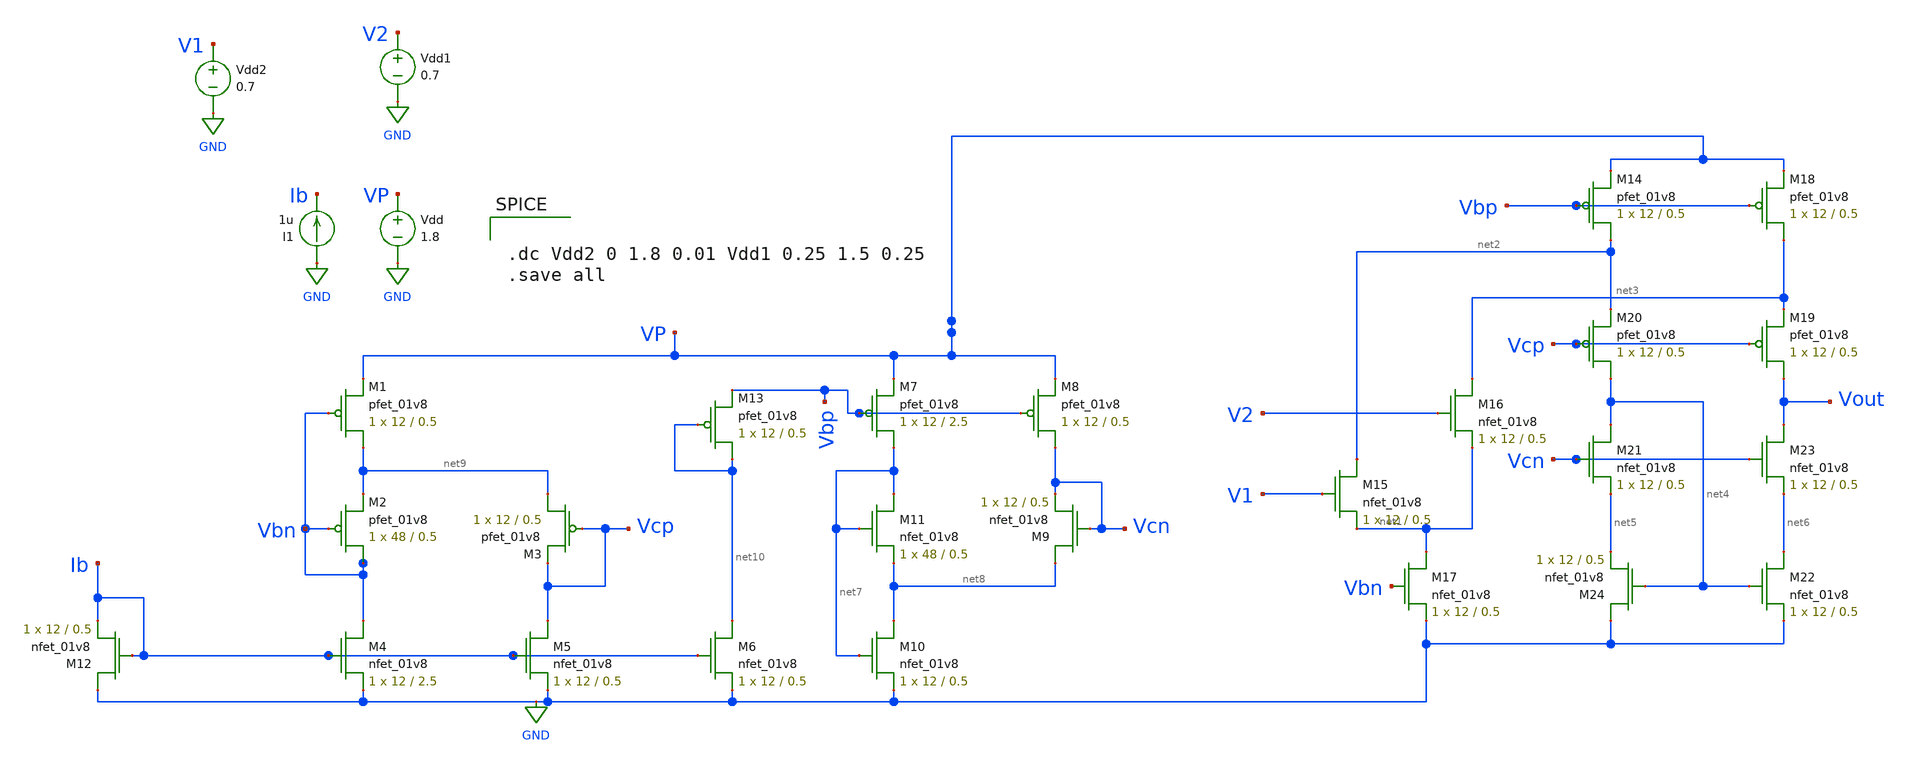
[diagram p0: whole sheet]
** sch_path: mp3/schematic/bias_circuit.sch
**.subckt bias_circuit
I1 GND Ib 1u
Vdd VP GND 1.8
XM14 net2 Vbp VP VDD sky130_fd_pr__pfet_01v8 L=0.5 W=12 nf=1 ad='int((nf+1)/2) * W/nf * 0.29' as='int((nf+2)/2) * W/nf * 0.29'
+ pd='2*int((nf+1)/2) * (W/nf + 0.29)' ps='2*int((nf+2)/2) * (W/nf + 0.29)' nrd='0.29 / W' nrs='0.29 / W'
+ sa=0 sb=0 sd=0 mult=1 m=1
XM15 net2 V1 net1 GND sky130_fd_pr__nfet_01v8 L=0.5 W=12 nf=1 ad='int((nf+1)/2) * W/nf * 0.29' as='int((nf+2)/2) * W/nf * 0.29'
+ pd='2*int((nf+1)/2) * (W/nf + 0.29)' ps='2*int((nf+2)/2) * (W/nf + 0.29)' nrd='0.29 / W' nrs='0.29 / W'
+ sa=0 sb=0 sd=0 mult=1 m=1
XM16 net3 V2 net1 GND sky130_fd_pr__nfet_01v8 L=0.5 W=12 nf=1 ad='int((nf+1)/2) * W/nf * 0.29' as='int((nf+2)/2) * W/nf * 0.29'
+ pd='2*int((nf+1)/2) * (W/nf + 0.29)' ps='2*int((nf+2)/2) * (W/nf + 0.29)' nrd='0.29 / W' nrs='0.29 / W'
+ sa=0 sb=0 sd=0 mult=1 m=1
XM17 net1 Vbn GND GND sky130_fd_pr__nfet_01v8 L=0.5 W=12 nf=1 ad='int((nf+1)/2) * W/nf * 0.29' as='int((nf+2)/2) * W/nf * 0.29'
+ pd='2*int((nf+1)/2) * (W/nf + 0.29)' ps='2*int((nf+2)/2) * (W/nf + 0.29)' nrd='0.29 / W' nrs='0.29 / W'
+ sa=0 sb=0 sd=0 mult=1 m=1
XM18 net3 Vbp VP VDD sky130_fd_pr__pfet_01v8 L=0.5 W=12 nf=1 ad='int((nf+1)/2) * W/nf * 0.29' as='int((nf+2)/2) * W/nf * 0.29'
+ pd='2*int((nf+1)/2) * (W/nf + 0.29)' ps='2*int((nf+2)/2) * (W/nf + 0.29)' nrd='0.29 / W' nrs='0.29 / W'
+ sa=0 sb=0 sd=0 mult=1 m=1
XM19 Vout Vcp net3 VDD sky130_fd_pr__pfet_01v8 L=0.5 W=12 nf=1 ad='int((nf+1)/2) * W/nf * 0.29' as='int((nf+2)/2) * W/nf * 0.29'
+ pd='2*int((nf+1)/2) * (W/nf + 0.29)' ps='2*int((nf+2)/2) * (W/nf + 0.29)' nrd='0.29 / W' nrs='0.29 / W'
+ sa=0 sb=0 sd=0 mult=1 m=1
XM20 net4 Vcp net2 VDD sky130_fd_pr__pfet_01v8 L=0.5 W=12 nf=1 ad='int((nf+1)/2) * W/nf * 0.29' as='int((nf+2)/2) * W/nf * 0.29'
+ pd='2*int((nf+1)/2) * (W/nf + 0.29)' ps='2*int((nf+2)/2) * (W/nf + 0.29)' nrd='0.29 / W' nrs='0.29 / W'
+ sa=0 sb=0 sd=0 mult=1 m=1
XM21 net4 Vcn net5 GND sky130_fd_pr__nfet_01v8 L=0.5 W=12 nf=1 ad='int((nf+1)/2) * W/nf * 0.29' as='int((nf+2)/2) * W/nf * 0.29'
+ pd='2*int((nf+1)/2) * (W/nf + 0.29)' ps='2*int((nf+2)/2) * (W/nf + 0.29)' nrd='0.29 / W' nrs='0.29 / W'
+ sa=0 sb=0 sd=0 mult=1 m=1
XM22 net6 net4 GND GND sky130_fd_pr__nfet_01v8 L=0.5 W=12 nf=1 ad='int((nf+1)/2) * W/nf * 0.29' as='int((nf+2)/2) * W/nf * 0.29'
+ pd='2*int((nf+1)/2) * (W/nf + 0.29)' ps='2*int((nf+2)/2) * (W/nf + 0.29)' nrd='0.29 / W' nrs='0.29 / W'
+ sa=0 sb=0 sd=0 mult=1 m=1
XM23 Vout Vcn net6 GND sky130_fd_pr__nfet_01v8 L=0.5 W=12 nf=1 ad='int((nf+1)/2) * W/nf * 0.29' as='int((nf+2)/2) * W/nf * 0.29'
+ pd='2*int((nf+1)/2) * (W/nf + 0.29)' ps='2*int((nf+2)/2) * (W/nf + 0.29)' nrd='0.29 / W' nrs='0.29 / W'
+ sa=0 sb=0 sd=0 mult=1 m=1
XM24 GND net4 net5 GND sky130_fd_pr__nfet_01v8 L=0.5 W=12 nf=1 ad='int((nf+1)/2) * W/nf * 0.29' as='int((nf+2)/2) * W/nf * 0.29'
+ pd='2*int((nf+1)/2) * (W/nf + 0.29)' ps='2*int((nf+2)/2) * (W/nf + 0.29)' nrd='0.29 / W' nrs='0.29 / W'
+ sa=0 sb=0 sd=0 mult=1 m=1
Vdd1 V2 GND 0.7
Vdd2 V1 GND 0.7
XM1 net9 Vbn VP VDD sky130_fd_pr__pfet_01v8 L=0.5 W=12 nf=1 ad='int((nf+1)/2) * W/nf * 0.29' as='int((nf+2)/2) * W/nf * 0.29'
+ pd='2*int((nf+1)/2) * (W/nf + 0.29)' ps='2*int((nf+2)/2) * (W/nf + 0.29)' nrd='0.29 / W' nrs='0.29 / W'
+ sa=0 sb=0 sd=0 mult=1 m=1
XM2 Vbn Vbn net9 VDD sky130_fd_pr__pfet_01v8 L=0.5 W=48 nf=1 ad='int((nf+1)/2) * W/nf * 0.29' as='int((nf+2)/2) * W/nf * 0.29'
+ pd='2*int((nf+1)/2) * (W/nf + 0.29)' ps='2*int((nf+2)/2) * (W/nf + 0.29)' nrd='0.29 / W' nrs='0.29 / W'
+ sa=0 sb=0 sd=0 mult=1 m=1
XM3 net9 Vcp Vcp VDD sky130_fd_pr__pfet_01v8 L=0.5 W=12 nf=1 ad='int((nf+1)/2) * W/nf * 0.29' as='int((nf+2)/2) * W/nf * 0.29'
+ pd='2*int((nf+1)/2) * (W/nf + 0.29)' ps='2*int((nf+2)/2) * (W/nf + 0.29)' nrd='0.29 / W' nrs='0.29 / W'
+ sa=0 sb=0 sd=0 mult=1 m=1
XM4 Vbn Ib GND GND sky130_fd_pr__nfet_01v8 L=2.5 W=12 nf=1 ad='int((nf+1)/2) * W/nf * 0.29' as='int((nf+2)/2) * W/nf * 0.29'
+ pd='2*int((nf+1)/2) * (W/nf + 0.29)' ps='2*int((nf+2)/2) * (W/nf + 0.29)' nrd='0.29 / W' nrs='0.29 / W'
+ sa=0 sb=0 sd=0 mult=1 m=1
XM5 Vcp Ib GND GND sky130_fd_pr__nfet_01v8 L=0.5 W=12 nf=1 ad='int((nf+1)/2) * W/nf * 0.29' as='int((nf+2)/2) * W/nf * 0.29'
+ pd='2*int((nf+1)/2) * (W/nf + 0.29)' ps='2*int((nf+2)/2) * (W/nf + 0.29)' nrd='0.29 / W' nrs='0.29 / W'
+ sa=0 sb=0 sd=0 mult=1 m=1
XM6 net10 Ib GND GND sky130_fd_pr__nfet_01v8 L=0.5 W=12 nf=1 ad='int((nf+1)/2) * W/nf * 0.29' as='int((nf+2)/2) * W/nf * 0.29'
+ pd='2*int((nf+1)/2) * (W/nf + 0.29)' ps='2*int((nf+2)/2) * (W/nf + 0.29)' nrd='0.29 / W' nrs='0.29 / W'
+ sa=0 sb=0 sd=0 mult=1 m=1
XM7 net7 Vbp VP VDD sky130_fd_pr__pfet_01v8 L=2.5 W=12 nf=1 ad='int((nf+1)/2) * W/nf * 0.29' as='int((nf+2)/2) * W/nf * 0.29'
+ pd='2*int((nf+1)/2) * (W/nf + 0.29)' ps='2*int((nf+2)/2) * (W/nf + 0.29)' nrd='0.29 / W' nrs='0.29 / W'
+ sa=0 sb=0 sd=0 mult=1 m=1
XM8 Vcn Vbp VP VDD sky130_fd_pr__pfet_01v8 L=0.5 W=12 nf=1 ad='int((nf+1)/2) * W/nf * 0.29' as='int((nf+2)/2) * W/nf * 0.29'
+ pd='2*int((nf+1)/2) * (W/nf + 0.29)' ps='2*int((nf+2)/2) * (W/nf + 0.29)' nrd='0.29 / W' nrs='0.29 / W'
+ sa=0 sb=0 sd=0 mult=1 m=1
XM9 net8 Vcn Vcn GND sky130_fd_pr__nfet_01v8 L=0.5 W=12 nf=1 ad='int((nf+1)/2) * W/nf * 0.29' as='int((nf+2)/2) * W/nf * 0.29'
+ pd='2*int((nf+1)/2) * (W/nf + 0.29)' ps='2*int((nf+2)/2) * (W/nf + 0.29)' nrd='0.29 / W' nrs='0.29 / W'
+ sa=0 sb=0 sd=0 mult=1 m=1
XM10 net8 net7 GND GND sky130_fd_pr__nfet_01v8 L=0.5 W=12 nf=1 ad='int((nf+1)/2) * W/nf * 0.29' as='int((nf+2)/2) * W/nf * 0.29'
+ pd='2*int((nf+1)/2) * (W/nf + 0.29)' ps='2*int((nf+2)/2) * (W/nf + 0.29)' nrd='0.29 / W' nrs='0.29 / W'
+ sa=0 sb=0 sd=0 mult=1 m=1
XM11 net7 net7 net8 GND sky130_fd_pr__nfet_01v8 L=0.5 W=48 nf=1 ad='int((nf+1)/2) * W/nf * 0.29' as='int((nf+2)/2) * W/nf * 0.29'
+ pd='2*int((nf+1)/2) * (W/nf + 0.29)' ps='2*int((nf+2)/2) * (W/nf + 0.29)' nrd='0.29 / W' nrs='0.29 / W'
+ sa=0 sb=0 sd=0 mult=1 m=1
XM12 GND Ib Ib GND sky130_fd_pr__nfet_01v8 L=0.5 W=12 nf=1 ad='int((nf+1)/2) * W/nf * 0.29' as='int((nf+2)/2) * W/nf * 0.29'
+ pd='2*int((nf+1)/2) * (W/nf + 0.29)' ps='2*int((nf+2)/2) * (W/nf + 0.29)' nrd='0.29 / W' nrs='0.29 / W'
+ sa=0 sb=0 sd=0 mult=1 m=1
XM13 net10 net10 Vbp VDD sky130_fd_pr__pfet_01v8 L=0.5 W=12 nf=1 ad='int((nf+1)/2) * W/nf * 0.29' as='int((nf+2)/2) * W/nf * 0.29'
+ pd='2*int((nf+1)/2) * (W/nf + 0.29)' ps='2*int((nf+2)/2) * (W/nf + 0.29)' nrd='0.29 / W' nrs='0.29 / W'
+ sa=0 sb=0 sd=0 mult=1 m=1
**** begin user architecture code

.option wnflag=1
.lib ~/skywater/skywater-pdk/libraries/sky130_fd_pr_ngspice/latest/models/sky130.lib.spice tt



.dc Vdd2 0 1.8 0.01 Vdd1 0.25 1.5 0.25
.save all

**** end user architecture code
**.ends
.GLOBAL GND
.end
